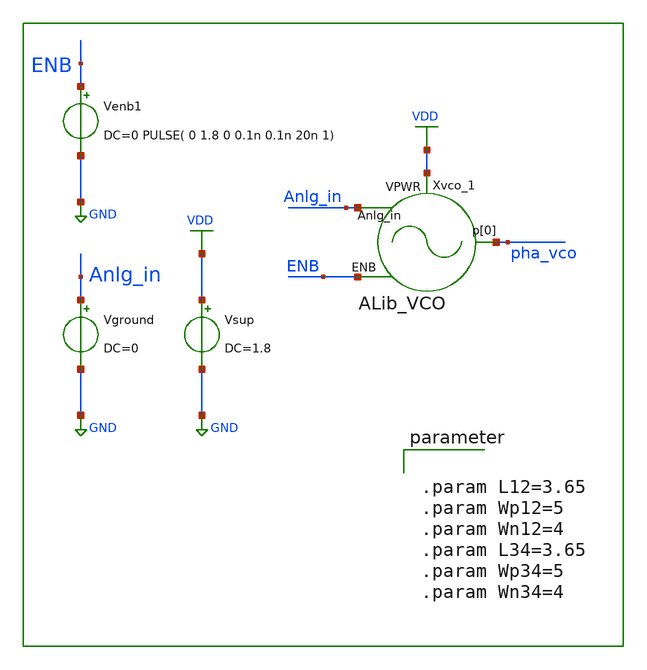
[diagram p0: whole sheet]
** sch_path: xschem/tb/VCO_tb.sch

.include $::SKYWATER_STDCELLS/sky130_fd_sc_hd.spice
.lib $::SKYWATER_MODELS/sky130.lib.spice tt

**.subckt VCO_tb
Vsup VDD GND DC=1.8
Vground Anlg_in GND DC=0
Venb1 ENB GND DC=0 PULSE( 0 1.8 0 0.1n 0.1n 20n 1)
Xvco_1 VDD pha_vco Anlg_in ENB ALib_VCO L12="L12" Wp12="Wp12" Wn12="Wn12" L34="L34" Wp34="Wp34"
+ Wn34="Wn34"
**** begin user architecture code


.param L12=3.65
.param Wp12=5
.param Wn12=4
.param L34=3.65
.param Wp34=5
.param Wn34=4


**** end user architecture code
**.ends
.GLOBAL VDD
.GLOBAL GND
**** begin user architecture code


.control
set nobreak
set num_threads=8
set test_mode = 1
* mode = 0: operation testing				1:  frequency extraction    2:  power consumption
if ($test_mode = 0)
    TRAN 1n 5u
    plot pha_vco
    MEAS TRAN prd TRIG pha_vco VAL=0.8 RISE=10 TARG pha_vco VAL=0.8 RISE=20
    let freq = 10/prd
    echo "frequency: "
    print freq
end
if ($test_mode = 1)
    let Vlow = 0
    let Vlimit = 1.01     $ set upper bound for sweeping
    let Vsweep = 0.2      $ set step size for sweeping
    let NoPoints=(Vlimit-Vlow)/Vsweep+2    $ set number of points for sweeping
    let freq =unitvec(NoPoints)
    let Vin  =unitvec(NoPoints)
    let Vin[0]=Vlow
    let ix=0
    while Vin[ix] < Vlimit
        alter Vground DC=Vin[ix]
        TRAN 0.4n 12u
        MEAS TRAN prd TRIG pha_vco VAL=0.8 RISE=10 TARG pha_vco VAL=0.8 RISE =20
        let freq[ix] = 10/prd
        let ix = ix+1
        Let Vin[ix] = Vin[ix-1]+Vsweep
    end
   print Vin freq
end
if ($test_mode = 2)
    save "vdd" @Vsup[i] "p[0]"
    TRAN 0.1n 5u
    MEAS TRAN I_vco AVG @Vsup[i] FROM=3u TO=4u
    MEAS TRAN V_vco AVG vdd FROM=3u TO=4u
    let Power=I_vco*V_vco
    print Power
end
.endc


**** end user architecture code
.end
